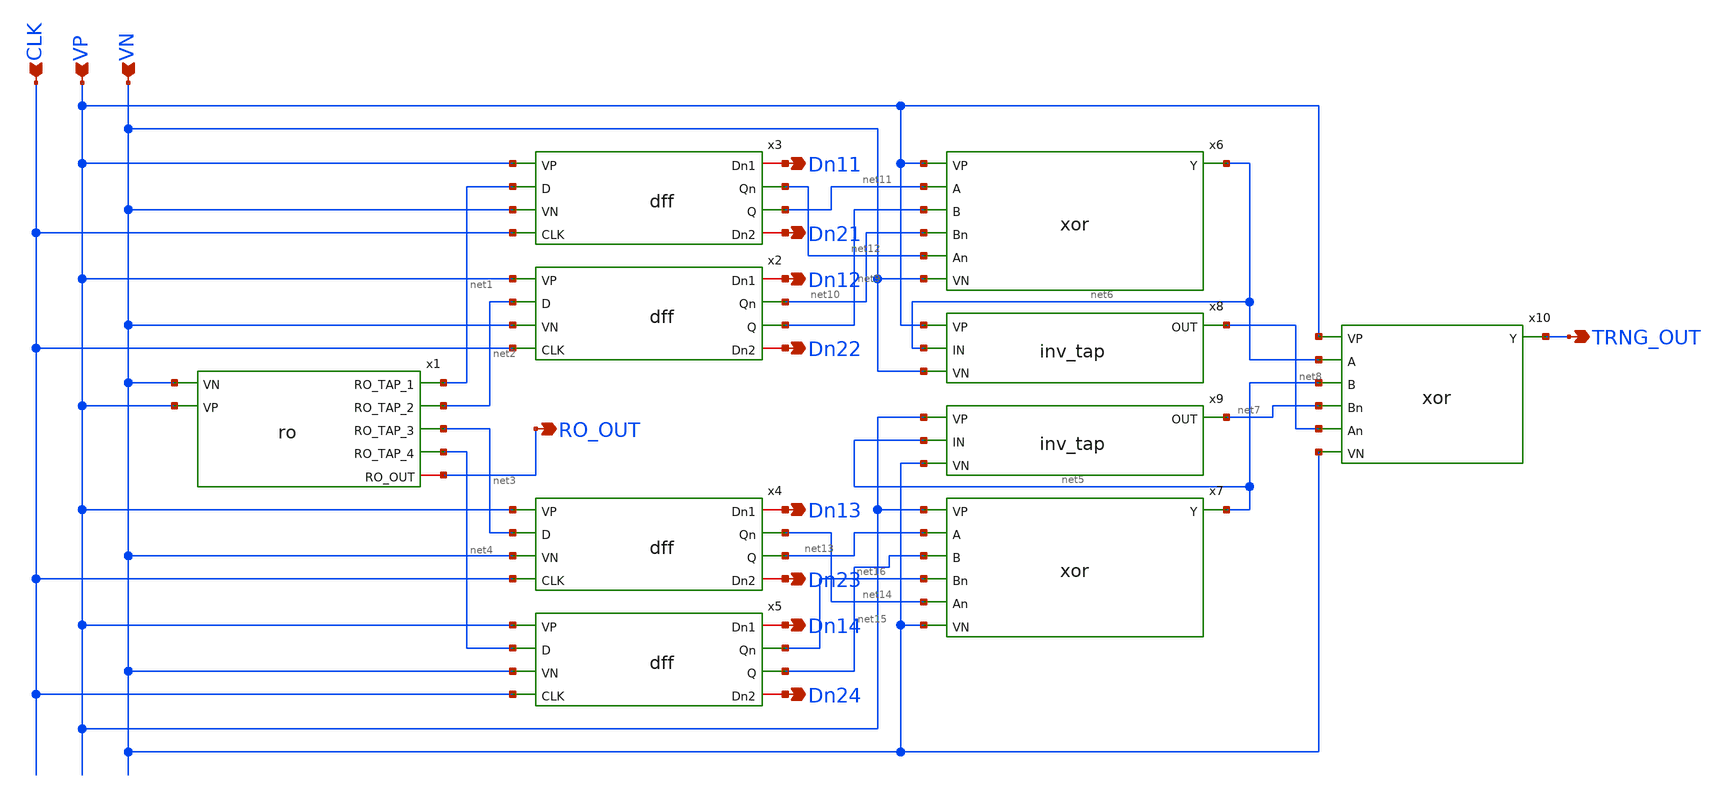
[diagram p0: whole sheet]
** sch_path: Mixed-Signal TRNG/xschem/trng.sch
**.subckt trng VP VN TRNG_OUT CLK RO_OUT Dn11 Dn21 Dn22 Dn23 Dn24 Dn12 Dn13 Dn14
*.ipin VP
*.ipin VN
*.opin TRNG_OUT
*.ipin CLK
*.opin RO_OUT
*.opin Dn11
*.opin Dn21
*.opin Dn22
*.opin Dn23
*.opin Dn24
*.opin Dn12
*.opin Dn13
*.opin Dn14
x2 VP Dn12 net10 net2 net9 Dn22 VN CLK dff
x3 VP Dn11 net12 net1 net11 Dn21 VN CLK dff
x4 VP Dn13 net14 net3 net13 Dn23 VN CLK dff
x5 VP Dn14 net16 net4 net15 Dn24 VN CLK dff
x6 VP net11 net9 net6 net10 net12 VN xor
x7 VP net13 net15 net5 net16 net14 VN xor
x8 VP net6 net8 VN inv_tap
x9 VP net5 net7 VN inv_tap
x10 VP net6 net5 TRNG_OUT net7 net8 VN xor
x1 net1 net2 net3 net4 RO_OUT VN VP ro
**.ends

* expanding   symbol:  /home/madvlsi/Desktop/Mixed-Signal TRNG/xschem/dff.sym # of pins=8
** sym_path: Mixed-Signal TRNG/xschem/dff.sym
** sch_path: Mixed-Signal TRNG/xschem/dff.sch
.subckt dff VP Dn1 Qn D Q Dn2 VN CLK
*.opin Qn
*.opin Q
*.ipin D
*.ipin CLK
*.ipin VP
*.ipin VN
*.iopin Dn2
*.iopin Dn1
XM1 net1 Dn1 VP VP sky130_fd_pr__pfet_01v8 L=0.15 W=2 nf=1 ad='int((nf+1)/2) * W/nf * 0.29' as='int((nf+2)/2) * W/nf * 0.29'
+ pd='2*int((nf+1)/2) * (W/nf + 0.29)' ps='2*int((nf+2)/2) * (W/nf + 0.29)' nrd='0.29 / W' nrs='0.29 / W'
+ sa=0 sb=0 sd=0 mult=1 m=1
XM2 net1 CLK VP VP sky130_fd_pr__pfet_01v8 L=0.15 W=4 nf=1 ad='int((nf+1)/2) * W/nf * 0.29' as='int((nf+2)/2) * W/nf * 0.29'
+ pd='2*int((nf+1)/2) * (W/nf + 0.29)' ps='2*int((nf+2)/2) * (W/nf + 0.29)' nrd='0.29 / W' nrs='0.29 / W'
+ sa=0 sb=0 sd=0 mult=1 m=1
XM3 net7 net10 net1 VP sky130_fd_pr__pfet_01v8 L=0.15 W=2 nf=1 ad='int((nf+1)/2) * W/nf * 0.29' as='int((nf+2)/2) * W/nf * 0.29'
+ pd='2*int((nf+1)/2) * (W/nf + 0.29)' ps='2*int((nf+2)/2) * (W/nf + 0.29)' nrd='0.29 / W' nrs='0.29 / W'
+ sa=0 sb=0 sd=0 mult=1 m=1
XM4 VP D net2 VP sky130_fd_pr__pfet_01v8 L=0.15 W=2 nf=1 ad='int((nf+1)/2) * W/nf * 0.29' as='int((nf+2)/2) * W/nf * 0.29'
+ pd='2*int((nf+1)/2) * (W/nf + 0.29)' ps='2*int((nf+2)/2) * (W/nf + 0.29)' nrd='0.29 / W' nrs='0.29 / W'
+ sa=0 sb=0 sd=0 mult=1 m=1
XM5 net2 CLK VP VP sky130_fd_pr__pfet_01v8 L=0.15 W=4 nf=1 ad='int((nf+1)/2) * W/nf * 0.29' as='int((nf+2)/2) * W/nf * 0.29'
+ pd='2*int((nf+1)/2) * (W/nf + 0.29)' ps='2*int((nf+2)/2) * (W/nf + 0.29)' nrd='0.29 / W' nrs='0.29 / W'
+ sa=0 sb=0 sd=0 mult=1 m=1
XM6 net10 net7 net2 VP sky130_fd_pr__pfet_01v8 L=0.15 W=2 nf=1 ad='int((nf+1)/2) * W/nf * 0.29' as='int((nf+2)/2) * W/nf * 0.29'
+ pd='2*int((nf+1)/2) * (W/nf + 0.29)' ps='2*int((nf+2)/2) * (W/nf + 0.29)' nrd='0.29 / W' nrs='0.29 / W'
+ sa=0 sb=0 sd=0 mult=1 m=1
XM7 VP net7 net3 VP sky130_fd_pr__pfet_01v8 L=0.15 W=2 nf=1 ad='int((nf+1)/2) * W/nf * 0.29' as='int((nf+2)/2) * W/nf * 0.29'
+ pd='2*int((nf+1)/2) * (W/nf + 0.29)' ps='2*int((nf+2)/2) * (W/nf + 0.29)' nrd='0.29 / W' nrs='0.29 / W'
+ sa=0 sb=0 sd=0 mult=1 m=1
XM8 Qn CLK net3 VP sky130_fd_pr__pfet_01v8 L=0.15 W=4 nf=1 ad='int((nf+1)/2) * W/nf * 0.29' as='int((nf+2)/2) * W/nf * 0.29'
+ pd='2*int((nf+1)/2) * (W/nf + 0.29)' ps='2*int((nf+2)/2) * (W/nf + 0.29)' nrd='0.29 / W' nrs='0.29 / W'
+ sa=0 sb=0 sd=0 mult=1 m=1
XM9 VP Q Qn VP sky130_fd_pr__pfet_01v8 L=0.15 W=4 nf=1 ad='int((nf+1)/2) * W/nf * 0.29' as='int((nf+2)/2) * W/nf * 0.29'
+ pd='2*int((nf+1)/2) * (W/nf + 0.29)' ps='2*int((nf+2)/2) * (W/nf + 0.29)' nrd='0.29 / W' nrs='0.29 / W'
+ sa=0 sb=0 sd=0 mult=1 m=1
XM10 net4 net10 VP VP sky130_fd_pr__pfet_01v8 L=0.15 W=2 nf=1 ad='int((nf+1)/2) * W/nf * 0.29' as='int((nf+2)/2) * W/nf * 0.29'
+ pd='2*int((nf+1)/2) * (W/nf + 0.29)' ps='2*int((nf+2)/2) * (W/nf + 0.29)' nrd='0.29 / W' nrs='0.29 / W'
+ sa=0 sb=0 sd=0 mult=1 m=1
XM11 Q CLK net4 VP sky130_fd_pr__pfet_01v8 L=0.15 W=4 nf=1 ad='int((nf+1)/2) * W/nf * 0.29' as='int((nf+2)/2) * W/nf * 0.29'
+ pd='2*int((nf+1)/2) * (W/nf + 0.29)' ps='2*int((nf+2)/2) * (W/nf + 0.29)' nrd='0.29 / W' nrs='0.29 / W'
+ sa=0 sb=0 sd=0 mult=1 m=1
XM12 VP Qn Q VP sky130_fd_pr__pfet_01v8 L=0.15 W=4 nf=1 ad='int((nf+1)/2) * W/nf * 0.29' as='int((nf+2)/2) * W/nf * 0.29'
+ pd='2*int((nf+1)/2) * (W/nf + 0.29)' ps='2*int((nf+2)/2) * (W/nf + 0.29)' nrd='0.29 / W' nrs='0.29 / W'
+ sa=0 sb=0 sd=0 mult=1 m=1
XM13 net9 D VN VN sky130_fd_pr__nfet_01v8 L=0.15 W=1 nf=1 ad='int((nf+1)/2) * W/nf * 0.29' as='int((nf+2)/2) * W/nf * 0.29'
+ pd='2*int((nf+1)/2) * (W/nf + 0.29)' ps='2*int((nf+2)/2) * (W/nf + 0.29)' nrd='0.29 / W' nrs='0.29 / W'
+ sa=0 sb=0 sd=0 mult=1 m=1
XM14 net9 CLK net10 VN sky130_fd_pr__nfet_01v8 L=0.15 W=2 nf=1 ad='int((nf+1)/2) * W/nf * 0.29' as='int((nf+2)/2) * W/nf * 0.29'
+ pd='2*int((nf+1)/2) * (W/nf + 0.29)' ps='2*int((nf+2)/2) * (W/nf + 0.29)' nrd='0.29 / W' nrs='0.29 / W'
+ sa=0 sb=0 sd=0 mult=1 m=1
XM15 VN net7 net10 VN sky130_fd_pr__nfet_01v8 L=0.15 W=1 nf=1 ad='int((nf+1)/2) * W/nf * 0.29' as='int((nf+2)/2) * W/nf * 0.29'
+ pd='2*int((nf+1)/2) * (W/nf + 0.29)' ps='2*int((nf+2)/2) * (W/nf + 0.29)' nrd='0.29 / W' nrs='0.29 / W'
+ sa=0 sb=0 sd=0 mult=1 m=1
XM16 VN net10 net5 VN sky130_fd_pr__nfet_01v8 L=0.15 W=1 nf=1 ad='int((nf+1)/2) * W/nf * 0.29' as='int((nf+2)/2) * W/nf * 0.29'
+ pd='2*int((nf+1)/2) * (W/nf + 0.29)' ps='2*int((nf+2)/2) * (W/nf + 0.29)' nrd='0.29 / W' nrs='0.29 / W'
+ sa=0 sb=0 sd=0 mult=1 m=1
XM17 VN CLK net5 VN sky130_fd_pr__nfet_01v8 L=0.15 W=2 nf=1 ad='int((nf+1)/2) * W/nf * 0.29' as='int((nf+2)/2) * W/nf * 0.29'
+ pd='2*int((nf+1)/2) * (W/nf + 0.29)' ps='2*int((nf+2)/2) * (W/nf + 0.29)' nrd='0.29 / W' nrs='0.29 / W'
+ sa=0 sb=0 sd=0 mult=1 m=1
XM18 Q Qn net5 VN sky130_fd_pr__nfet_01v8 L=0.15 W=2 nf=1 ad='int((nf+1)/2) * W/nf * 0.29' as='int((nf+2)/2) * W/nf * 0.29'
+ pd='2*int((nf+1)/2) * (W/nf + 0.29)' ps='2*int((nf+2)/2) * (W/nf + 0.29)' nrd='0.29 / W' nrs='0.29 / W'
+ sa=0 sb=0 sd=0 mult=1 m=1
XM19 VN Dn2 net8 VN sky130_fd_pr__nfet_01v8 L=0.15 W=1 nf=1 ad='int((nf+1)/2) * W/nf * 0.29' as='int((nf+2)/2) * W/nf * 0.29'
+ pd='2*int((nf+1)/2) * (W/nf + 0.29)' ps='2*int((nf+2)/2) * (W/nf + 0.29)' nrd='0.29 / W' nrs='0.29 / W'
+ sa=0 sb=0 sd=0 mult=1 m=1
XM20 net8 CLK net7 VN sky130_fd_pr__nfet_01v8 L=0.15 W=2 nf=1 ad='int((nf+1)/2) * W/nf * 0.29' as='int((nf+2)/2) * W/nf * 0.29'
+ pd='2*int((nf+1)/2) * (W/nf + 0.29)' ps='2*int((nf+2)/2) * (W/nf + 0.29)' nrd='0.29 / W' nrs='0.29 / W'
+ sa=0 sb=0 sd=0 mult=1 m=1
XM21 VN net10 net7 VN sky130_fd_pr__nfet_01v8 L=0.15 W=1 nf=1 ad='int((nf+1)/2) * W/nf * 0.29' as='int((nf+2)/2) * W/nf * 0.29'
+ pd='2*int((nf+1)/2) * (W/nf + 0.29)' ps='2*int((nf+2)/2) * (W/nf + 0.29)' nrd='0.29 / W' nrs='0.29 / W'
+ sa=0 sb=0 sd=0 mult=1 m=1
XM22 net6 net7 VN VN sky130_fd_pr__nfet_01v8 L=0.15 W=1 nf=1 ad='int((nf+1)/2) * W/nf * 0.29' as='int((nf+2)/2) * W/nf * 0.29'
+ pd='2*int((nf+1)/2) * (W/nf + 0.29)' ps='2*int((nf+2)/2) * (W/nf + 0.29)' nrd='0.29 / W' nrs='0.29 / W'
+ sa=0 sb=0 sd=0 mult=1 m=1
XM23 VN CLK net6 VN sky130_fd_pr__nfet_01v8 L=0.15 W=2 nf=1 ad='int((nf+1)/2) * W/nf * 0.29' as='int((nf+2)/2) * W/nf * 0.29'
+ pd='2*int((nf+1)/2) * (W/nf + 0.29)' ps='2*int((nf+2)/2) * (W/nf + 0.29)' nrd='0.29 / W' nrs='0.29 / W'
+ sa=0 sb=0 sd=0 mult=1 m=1
XM24 Qn Q net6 VN sky130_fd_pr__nfet_01v8 L=0.15 W=2 nf=1 ad='int((nf+1)/2) * W/nf * 0.29' as='int((nf+2)/2) * W/nf * 0.29'
+ pd='2*int((nf+1)/2) * (W/nf + 0.29)' ps='2*int((nf+2)/2) * (W/nf + 0.29)' nrd='0.29 / W' nrs='0.29 / W'
+ sa=0 sb=0 sd=0 mult=1 m=1
.ends


* expanding   symbol:  /home/madvlsi/Desktop/Mixed-Signal TRNG/xschem/xor.sym # of pins=7
** sym_path: Mixed-Signal TRNG/xschem/xor.sym
** sch_path: Mixed-Signal TRNG/xschem/xor.sch
.subckt xor VP A B Y Bn An VN
*.ipin B
*.ipin Bn
*.ipin A
*.ipin An
*.opin Y
*.ipin VP
*.ipin VN
XM3 net1 Bn An VP sky130_fd_pr__pfet_01v8 L=0.15 W=4 nf=1 ad='int((nf+1)/2) * W/nf * 0.29' as='int((nf+2)/2) * W/nf * 0.29'
+ pd='2*int((nf+1)/2) * (W/nf + 0.29)' ps='2*int((nf+2)/2) * (W/nf + 0.29)' nrd='0.29 / W' nrs='0.29 / W'
+ sa=0 sb=0 sd=0 mult=1 m=1
XM4 net1 B An VN sky130_fd_pr__nfet_01v8 L=0.15 W=2 nf=1 ad='int((nf+1)/2) * W/nf * 0.29' as='int((nf+2)/2) * W/nf * 0.29'
+ pd='2*int((nf+1)/2) * (W/nf + 0.29)' ps='2*int((nf+2)/2) * (W/nf + 0.29)' nrd='0.29 / W' nrs='0.29 / W'
+ sa=0 sb=0 sd=0 mult=1 m=1
XM5 net2 net1 VP VP sky130_fd_pr__pfet_01v8 L=0.15 W=4 nf=1 ad='int((nf+1)/2) * W/nf * 0.29' as='int((nf+2)/2) * W/nf * 0.29'
+ pd='2*int((nf+1)/2) * (W/nf + 0.29)' ps='2*int((nf+2)/2) * (W/nf + 0.29)' nrd='0.29 / W' nrs='0.29 / W'
+ sa=0 sb=0 sd=0 mult=1 m=1
XM6 net2 net1 VN VN sky130_fd_pr__nfet_01v8 L=0.15 W=2 nf=1 ad='int((nf+1)/2) * W/nf * 0.29' as='int((nf+2)/2) * W/nf * 0.29'
+ pd='2*int((nf+1)/2) * (W/nf + 0.29)' ps='2*int((nf+2)/2) * (W/nf + 0.29)' nrd='0.29 / W' nrs='0.29 / W'
+ sa=0 sb=0 sd=0 mult=1 m=1
XM1 net1 B A VP sky130_fd_pr__pfet_01v8 L=0.15 W=4 nf=1 ad='int((nf+1)/2) * W/nf * 0.29' as='int((nf+2)/2) * W/nf * 0.29'
+ pd='2*int((nf+1)/2) * (W/nf + 0.29)' ps='2*int((nf+2)/2) * (W/nf + 0.29)' nrd='0.29 / W' nrs='0.29 / W'
+ sa=0 sb=0 sd=0 mult=1 m=1
XM2 net1 Bn A VN sky130_fd_pr__nfet_01v8 L=0.15 W=2 nf=1 ad='int((nf+1)/2) * W/nf * 0.29' as='int((nf+2)/2) * W/nf * 0.29'
+ pd='2*int((nf+1)/2) * (W/nf + 0.29)' ps='2*int((nf+2)/2) * (W/nf + 0.29)' nrd='0.29 / W' nrs='0.29 / W'
+ sa=0 sb=0 sd=0 mult=1 m=1
XM7 Y net2 VP VP sky130_fd_pr__pfet_01v8 L=0.15 W=4 nf=1 ad='int((nf+1)/2) * W/nf * 0.29' as='int((nf+2)/2) * W/nf * 0.29'
+ pd='2*int((nf+1)/2) * (W/nf + 0.29)' ps='2*int((nf+2)/2) * (W/nf + 0.29)' nrd='0.29 / W' nrs='0.29 / W'
+ sa=0 sb=0 sd=0 mult=1 m=1
XM8 Y net2 VN VN sky130_fd_pr__nfet_01v8 L=0.15 W=2 nf=1 ad='int((nf+1)/2) * W/nf * 0.29' as='int((nf+2)/2) * W/nf * 0.29'
+ pd='2*int((nf+1)/2) * (W/nf + 0.29)' ps='2*int((nf+2)/2) * (W/nf + 0.29)' nrd='0.29 / W' nrs='0.29 / W'
+ sa=0 sb=0 sd=0 mult=1 m=1
.ends


* expanding   symbol:  /home/madvlsi/Desktop/Mixed-Signal TRNG/xschem/inv_tap.sym # of pins=4
** sym_path: Mixed-Signal TRNG/xschem/inv_tap.sym
** sch_path: Mixed-Signal TRNG/xschem/inv_tap.sch
.subckt inv_tap VP IN OUT VN
*.ipin IN
*.opin OUT
*.ipin VP
*.ipin VN
XM1 OUT IN VN VN sky130_fd_pr__nfet_01v8 L=0.15 W=0.6 nf=1 ad='int((nf+1)/2) * W/nf * 0.29' as='int((nf+2)/2) * W/nf * 0.29'
+ pd='2*int((nf+1)/2) * (W/nf + 0.29)' ps='2*int((nf+2)/2) * (W/nf + 0.29)' nrd='0.29 / W' nrs='0.29 / W'
+ sa=0 sb=0 sd=0 mult=1 m=1
XM2 OUT IN VP VP sky130_fd_pr__pfet_01v8 L=0.15 W=1.2 nf=1 ad='int((nf+1)/2) * W/nf * 0.29' as='int((nf+2)/2) * W/nf * 0.29'
+ pd='2*int((nf+1)/2) * (W/nf + 0.29)' ps='2*int((nf+2)/2) * (W/nf + 0.29)' nrd='0.29 / W' nrs='0.29 / W'
+ sa=0 sb=0 sd=0 mult=1 m=1
.ends


* expanding   symbol:  /home/madvlsi/Desktop/Mixed-Signal TRNG/xschem/ro.sym # of pins=7
** sym_path: Mixed-Signal TRNG/xschem/ro.sym
** sch_path: Mixed-Signal TRNG/xschem/ro.sch
.subckt ro RO_TAP_1 RO_TAP_2 RO_TAP_3 RO_TAP_4 RO_OUT VN VP
*.iopin RO_OUT
*.ipin VP
*.ipin VN
*.opin RO_TAP_1
*.opin RO_TAP_2
*.opin RO_TAP_3
*.opin RO_TAP_4
x1 VP RO_OUT net1 VN inv
x2 VP net1 net2 VN inv
x3 VP net2 net3 VN inv
x4 VP net3 net4 VN inv
x5 VP net4 RO_OUT VN inv
x6 VP net1 RO_TAP_1 VN inv_tap
x7 VP net2 RO_TAP_2 VN inv_tap
x8 VP net3 RO_TAP_3 VN inv_tap
x9 VP net4 RO_TAP_4 VN inv_tap
.ends


* expanding   symbol:  /home/madvlsi/Desktop/Mixed-Signal TRNG/xschem/inv.sym # of pins=4
** sym_path: Mixed-Signal TRNG/xschem/inv.sym
** sch_path: Mixed-Signal TRNG/xschem/inv.sch
.subckt inv VP IN OUT VN
*.ipin IN
*.opin OUT
*.ipin VP
*.ipin VN
XM1 OUT IN VN VN sky130_fd_pr__nfet_01v8 L=0.15 W=2 nf=1 ad='int((nf+1)/2) * W/nf * 0.29' as='int((nf+2)/2) * W/nf * 0.29'
+ pd='2*int((nf+1)/2) * (W/nf + 0.29)' ps='2*int((nf+2)/2) * (W/nf + 0.29)' nrd='0.29 / W' nrs='0.29 / W'
+ sa=0 sb=0 sd=0 mult=1 m=1
XM2 OUT IN VP VP sky130_fd_pr__pfet_01v8 L=0.15 W=4 nf=1 ad='int((nf+1)/2) * W/nf * 0.29' as='int((nf+2)/2) * W/nf * 0.29'
+ pd='2*int((nf+1)/2) * (W/nf + 0.29)' ps='2*int((nf+2)/2) * (W/nf + 0.29)' nrd='0.29 / W' nrs='0.29 / W'
+ sa=0 sb=0 sd=0 mult=1 m=1
.ends

.end
